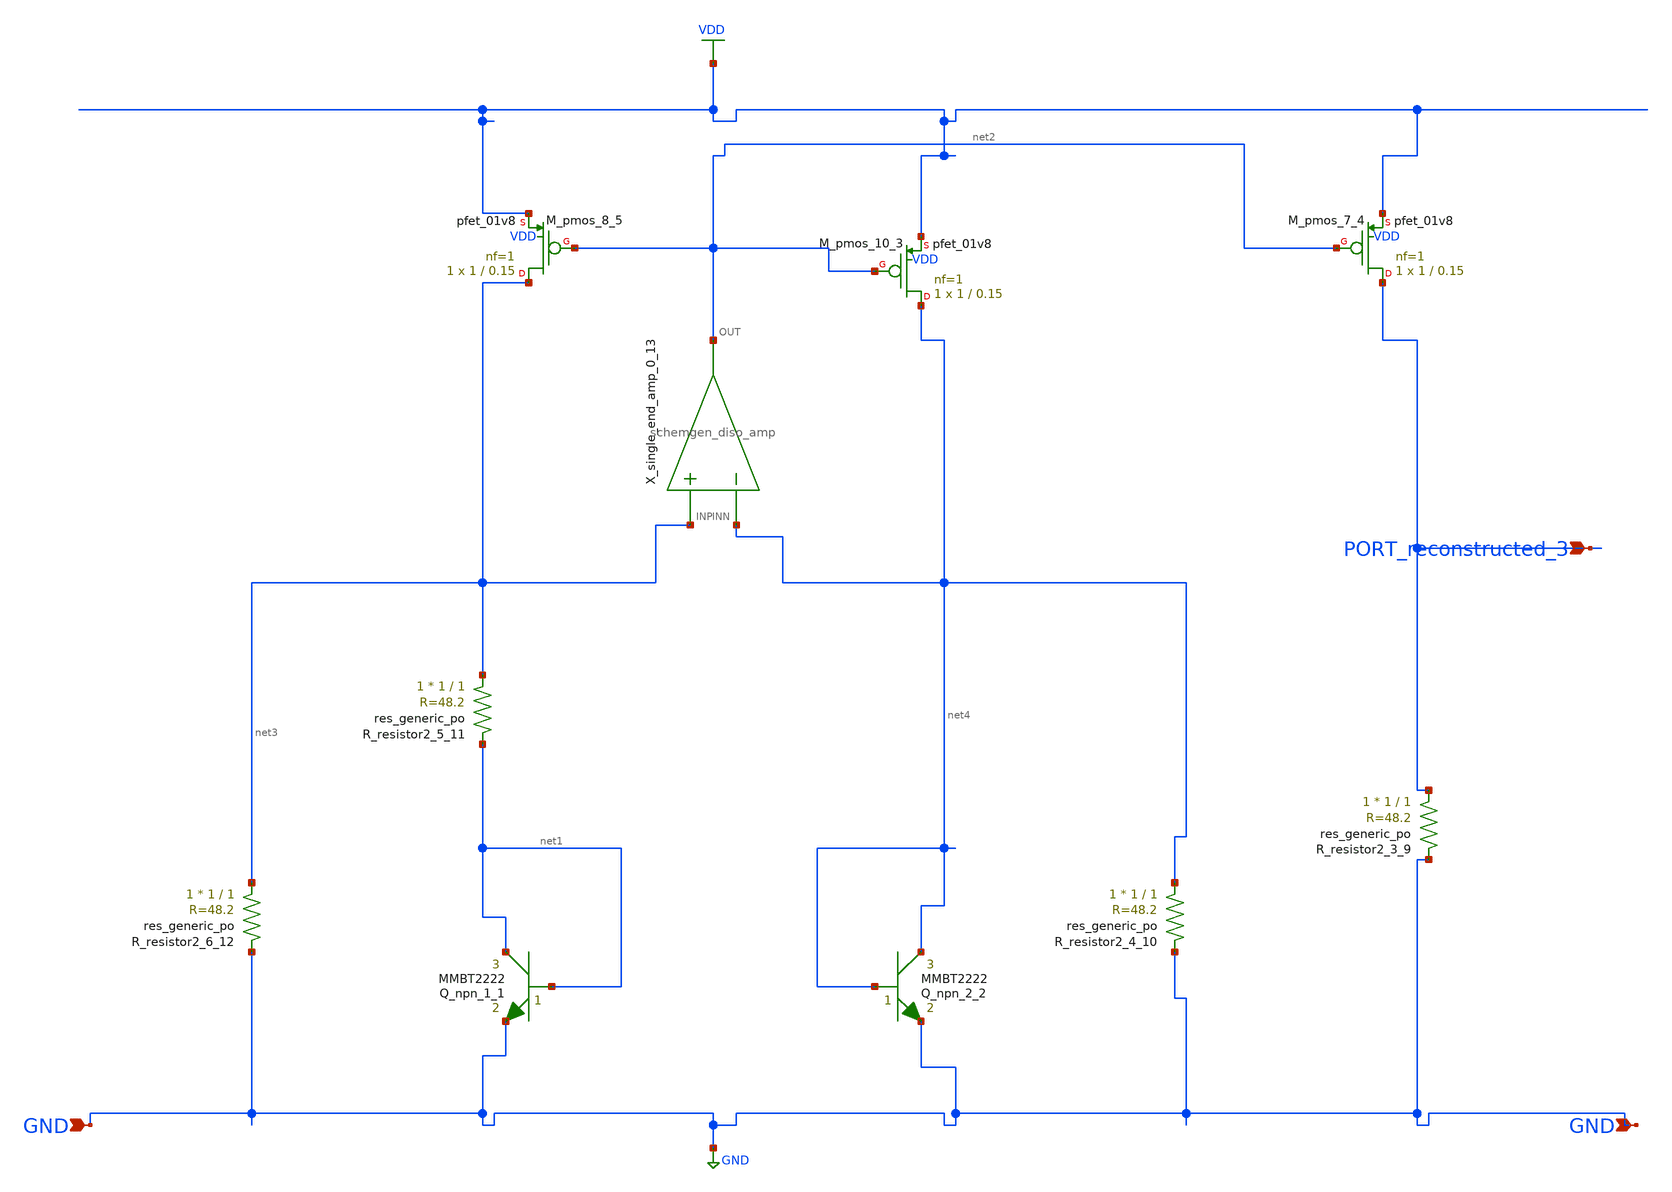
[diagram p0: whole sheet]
** sch_path: schematics/Image2Net/114.sch
**.subckt 114 PORT_reconstructed_3 GND GND
*.ipin PORT_reconstructed_3
*.ipin GND
*.ipin GND
Q_npn_1_1 net1 net1 GND MMBT2222 area=1 m=1
Q_npn_2_2 net4 net4 GND MMBT2222 area=1 m=1
XM_pmos_10_3 net4 net2 VDD VDD sky130_fd_pr__pfet_01v8 L=0.15 W=1 nf=1 ad='int((1 + 1)/2) * 1 / 1 * 0.29'
+ as='int((1 + 2)/2) * 1 / 1 * 0.29' pd='2*int((1 + 1)/2) * (1 / 1 + 0.29)' ps='2*int((1 + 2)/2) * (1 / 1 + 0.29)'
+ nrd='0.29 / 1 ' nrs='0.29 / 1 ' sa=0 sb=0 sd=0 mult=1 m=1
XM_pmos_7_4 PORT_reconstructed_3 net2 VDD VDD sky130_fd_pr__pfet_01v8 L=0.15 W=1 nf=1 ad='int((1 + 1)/2) * 1 / 1 * 0.29'
+ as='int((1 + 2)/2) * 1 / 1 * 0.29' pd='2*int((1 + 1)/2) * (1 / 1 + 0.29)' ps='2*int((1 + 2)/2) * (1 / 1 + 0.29)'
+ nrd='0.29 / 1 ' nrs='0.29 / 1 ' sa=0 sb=0 sd=0 mult=1 m=1
XM_pmos_8_5 net3 net2 VDD VDD sky130_fd_pr__pfet_01v8 L=0.15 W=1 nf=1 ad='int((1 + 1)/2) * 1 / 1 * 0.29'
+ as='int((1 + 2)/2) * 1 / 1 * 0.29' pd='2*int((1 + 1)/2) * (1 / 1 + 0.29)' ps='2*int((1 + 2)/2) * (1 / 1 + 0.29)'
+ nrd='0.29 / 1 ' nrs='0.29 / 1 ' sa=0 sb=0 sd=0 mult=1 m=1
XR_resistor2_3_9 PORT_reconstructed_3 GND sky130_fd_pr__res_generic_po W=1 L=1 m=1
XR_resistor2_4_10 net4 GND sky130_fd_pr__res_generic_po W=1 L=1 m=1
XR_resistor2_5_11 net3 net1 sky130_fd_pr__res_generic_po W=1 L=1 m=1
XR_resistor2_6_12 net3 GND sky130_fd_pr__res_generic_po W=1 L=1 m=1
X_single_end_amp_0_13 net3 net4 net2 schemgen_diso_amp
**.ends

* expanding   symbol:  schemgen_diso_amp.sym # of pins=3
** sym_path: symbols/schemgen_diso_amp.sym
.subckt schemgen_diso_amp INP INN OUT
* SchemGen ideal op-amp: Vout = 1e5 * (V(INP) - V(INN))
E1 OUT 0 INP INN 1e5
.ends schemgen_diso_amp
.GLOBAL GND
.GLOBAL VDD
.end
